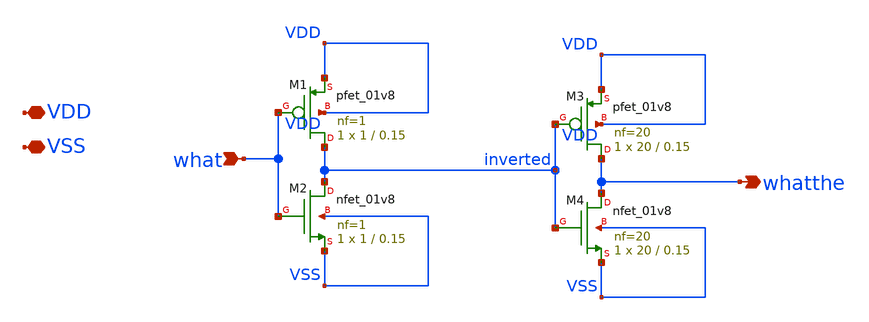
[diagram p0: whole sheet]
** sch_path: xschem/double_inverter.sch
**.subckt double_inverter VDD VSS what whatthe
*.iopin VDD
*.iopin VSS
*.ipin what
*.opin whatthe
XM1 inverted what VDD VDD sky130_fd_pr__pfet_01v8 L=0.15 W=1 nf=1 ad='int((nf+1)/2) * W/nf * 0.29' as='int((nf+2)/2) * W/nf * 0.29'
+ pd='2*int((nf+1)/2) * (W/nf + 0.29)' ps='2*int((nf+2)/2) * (W/nf + 0.29)' nrd='0.29 / W' nrs='0.29 / W'
+ sa=0 sb=0 sd=0 mult=1 m=1
XM2 inverted what VSS VSS sky130_fd_pr__nfet_01v8 L=0.15 W=1 nf=1 ad='int((nf+1)/2) * W/nf * 0.29' as='int((nf+2)/2) * W/nf * 0.29'
+ pd='2*int((nf+1)/2) * (W/nf + 0.29)' ps='2*int((nf+2)/2) * (W/nf + 0.29)' nrd='0.29 / W' nrs='0.29 / W'
+ sa=0 sb=0 sd=0 mult=1 m=1
XM3 whatthe inverted VDD VDD sky130_fd_pr__pfet_01v8 L=0.15 W=20 nf=20 ad='int((nf+1)/2) * W/nf * 0.29'
+ as='int((nf+2)/2) * W/nf * 0.29' pd='2*int((nf+1)/2) * (W/nf + 0.29)' ps='2*int((nf+2)/2) * (W/nf + 0.29)'
+ nrd='0.29 / W' nrs='0.29 / W' sa=0 sb=0 sd=0 mult=1 m=1
XM4 whatthe inverted VSS VSS sky130_fd_pr__nfet_01v8 L=0.15 W=20 nf=20 ad='int((nf+1)/2) * W/nf * 0.29'
+ as='int((nf+2)/2) * W/nf * 0.29' pd='2*int((nf+1)/2) * (W/nf + 0.29)' ps='2*int((nf+2)/2) * (W/nf + 0.29)'
+ nrd='0.29 / W' nrs='0.29 / W' sa=0 sb=0 sd=0 mult=1 m=1
**.ends
.end
